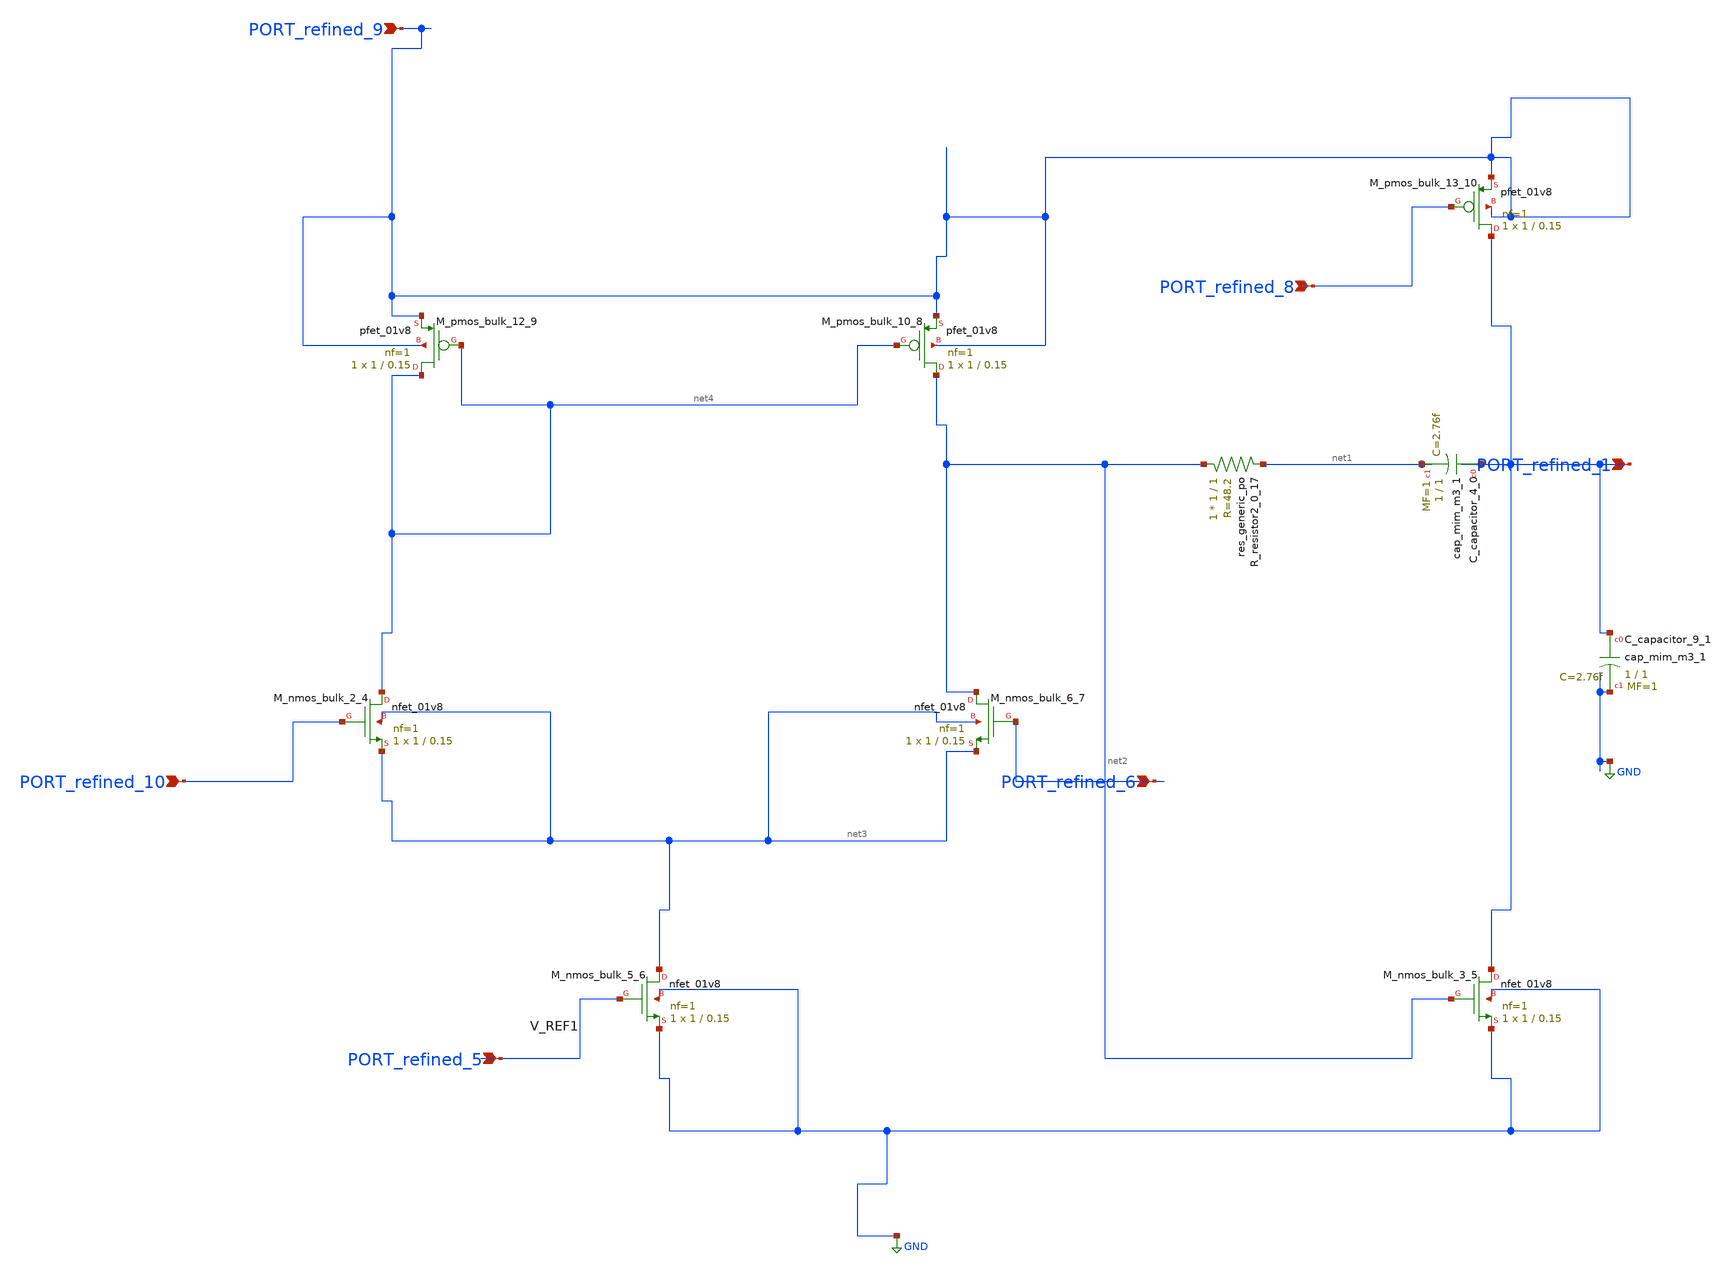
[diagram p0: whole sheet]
** sch_path: schematics/p02_two_stage_opamp.sch
**.subckt p02_two_stage_opamp PORT_refined_1 PORT_refined_6 PORT_refined_9 PORT_refined_8
*+ PORT_refined_5 PORT_refined_10
*.ipin PORT_refined_1
*.ipin PORT_refined_6
*.ipin PORT_refined_9
*.ipin PORT_refined_8
*.ipin PORT_refined_5
*.ipin PORT_refined_10
XC_capacitor_4_0 PORT_refined_1 net1 sky130_fd_pr__cap_mim_m3_1 W=1 L=1 MF=1 m=1
XC_capacitor_9_1 PORT_refined_1 GND sky130_fd_pr__cap_mim_m3_1 W=1 L=1 MF=1 m=1
XM_nmos_bulk_2_4 net4 PORT_refined_10 net3 net3 sky130_fd_pr__nfet_01v8 L=0.15 W=1 nf=1 ad='int((1 + 1)/2) * 1 / 1 * 0.29'
+ as='int((1 + 2)/2) * 1 / 1 * 0.29' pd='2*int((1 + 1)/2) * (1 / 1 + 0.29)' ps='2*int((1 + 2)/2) * (1 / 1 + 0.29)'
+ nrd='0.29 / 1 ' nrs='0.29 / 1 ' sa=0 sb=0 sd=0 mult=1 m=1
XM_nmos_bulk_3_5 PORT_refined_1 net2 GND GND sky130_fd_pr__nfet_01v8 L=0.15 W=1 nf=1 ad='int((1 + 1)/2) * 1 / 1 * 0.29'
+ as='int((1 + 2)/2) * 1 / 1 * 0.29' pd='2*int((1 + 1)/2) * (1 / 1 + 0.29)' ps='2*int((1 + 2)/2) * (1 / 1 + 0.29)'
+ nrd='0.29 / 1 ' nrs='0.29 / 1 ' sa=0 sb=0 sd=0 mult=1 m=1
XM_nmos_bulk_5_6 net3 PORT_refined_5 GND GND sky130_fd_pr__nfet_01v8 L=0.15 W=1 nf=1 ad='int((1 + 1)/2) * 1 / 1 * 0.29'
+ as='int((1 + 2)/2) * 1 / 1 * 0.29' pd='2*int((1 + 1)/2) * (1 / 1 + 0.29)' ps='2*int((1 + 2)/2) * (1 / 1 + 0.29)'
+ nrd='0.29 / 1 ' nrs='0.29 / 1 ' sa=0 sb=0 sd=0 mult=1 m=1
XM_nmos_bulk_6_7 net2 PORT_refined_6 net3 net3 sky130_fd_pr__nfet_01v8 L=0.15 W=1 nf=1 ad='int((1 + 1)/2) * 1 / 1 * 0.29'
+ as='int((1 + 2)/2) * 1 / 1 * 0.29' pd='2*int((1 + 1)/2) * (1 / 1 + 0.29)' ps='2*int((1 + 2)/2) * (1 / 1 + 0.29)'
+ nrd='0.29 / 1 ' nrs='0.29 / 1 ' sa=0 sb=0 sd=0 mult=1 m=1
XM_pmos_bulk_10_8 net2 net4 PORT_refined_9 PORT_refined_9 sky130_fd_pr__pfet_01v8 L=0.15 W=1 nf=1 ad='int((1 + 1)/2) * 1 / 1 * 0.29'
+ as='int((1 + 2)/2) * 1 / 1 * 0.29' pd='2*int((1 + 1)/2) * (1 / 1 + 0.29)' ps='2*int((1 + 2)/2) * (1 / 1 + 0.29)'
+ nrd='0.29 / 1 ' nrs='0.29 / 1 ' sa=0 sb=0 sd=0 mult=1 m=1
XM_pmos_bulk_12_9 net4 net4 PORT_refined_9 PORT_refined_9 sky130_fd_pr__pfet_01v8 L=0.15 W=1 nf=1 ad='int((1 + 1)/2) * 1 / 1 * 0.29'
+ as='int((1 + 2)/2) * 1 / 1 * 0.29' pd='2*int((1 + 1)/2) * (1 / 1 + 0.29)' ps='2*int((1 + 2)/2) * (1 / 1 + 0.29)'
+ nrd='0.29 / 1 ' nrs='0.29 / 1 ' sa=0 sb=0 sd=0 mult=1 m=1
XM_pmos_bulk_13_10 PORT_refined_1 PORT_refined_8 PORT_refined_9 PORT_refined_9 sky130_fd_pr__pfet_01v8
+ L=0.15 W=1 nf=1 ad='int((1 + 1)/2) * 1 / 1 * 0.29' as='int((1 + 2)/2) * 1 / 1 * 0.29' pd='2*int((1 + 1)/2) * (1 / 1 + 0.29)'
+ ps='2*int((1 + 2)/2) * (1 / 1 + 0.29)' nrd='0.29 / 1 ' nrs='0.29 / 1 ' sa=0 sb=0 sd=0 mult=1 m=1
XR_resistor2_0_17 net2 net1 sky130_fd_pr__res_generic_po W=1 L=1 m=1
**.ends
.GLOBAL GND
.end
